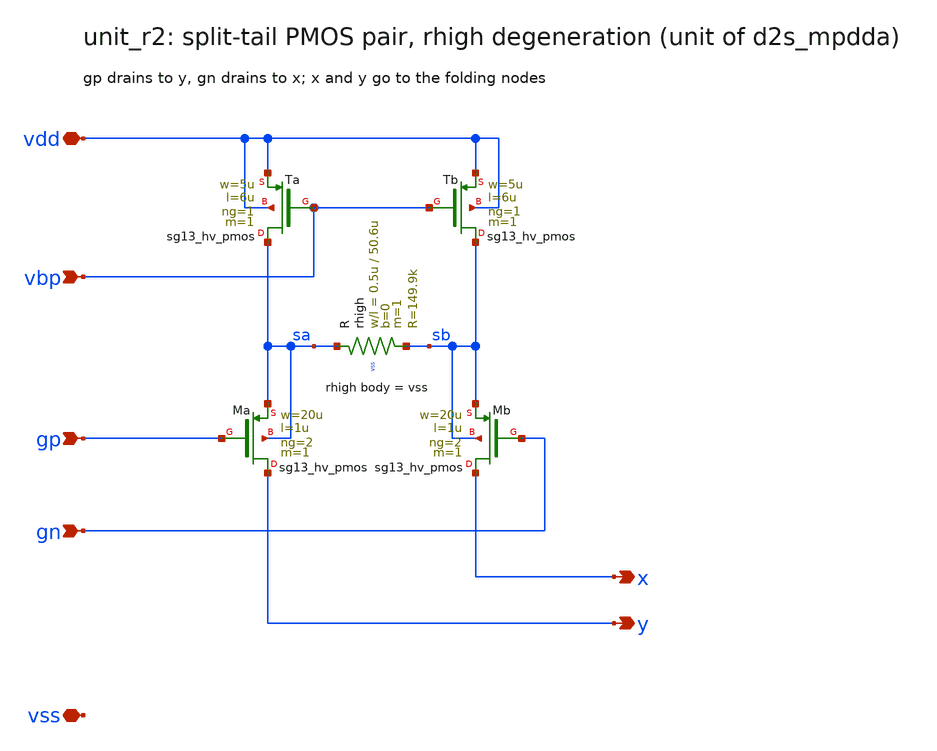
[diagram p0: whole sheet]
** sch_path: sudelbuecher/design_considerations/class_ab_pad_driver/improvements/xschem/unit_r2.sch
**.subckt unit_r2 x y gp gn vdd vss vbp
*.opin x
*.opin y
*.ipin gp
*.ipin gn
*.iopin vdd
*.iopin vss
*.ipin vbp
XTa sa vbp vdd vdd sg13_hv_pmos w=5u l=6u ng=1 m=1 mm_ok=1
XTb sb vbp vdd vdd sg13_hv_pmos w=5u l=6u ng=1 m=1 mm_ok=1
XMa y gp sa sa sg13_hv_pmos w=20u l=1u ng=2 m=1 mm_ok=1
XMb x gn sb sb sg13_hv_pmos w=20u l=1u ng=2 m=1 mm_ok=1
XR sa sb vss rhigh w=0.5u l=50.6u m=1 b=0 mm_ok=1
**.ends
.end
